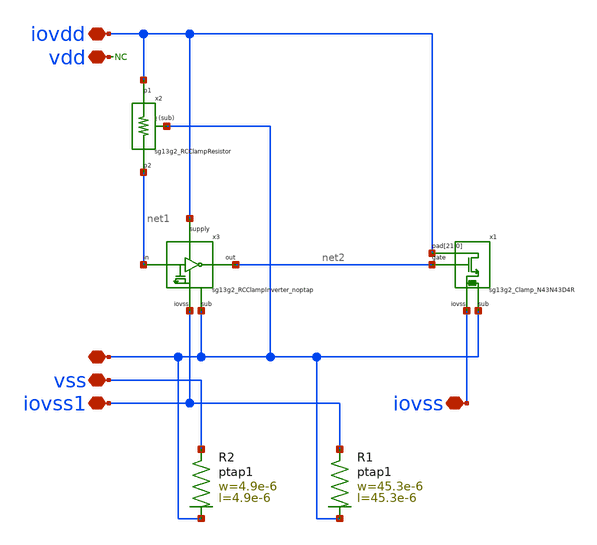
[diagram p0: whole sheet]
** sch_path: MSPHY6034-main/dependencies/unic_cass_2025_team04_padring/xschem/openpdk-libraries/ihp-sg13g2/sg13g2_io/xschem/sg13g2_IOPadIOVddAccess.sch
**.subckt sg13g2_IOPadIOVddAccess iovdd vss vdd ! iovss1 iovss
*.iopin iovdd
*.iopin vss
*.iopin vdd
*.iopin !
*.iopin iovss1
*.iopin iovss
XR2 vss ! ptap1 R=22.47 w=4.9e-6 l=4.9e-6
* noconn vdd
XR1 iovss1 ! ptap1 R=438.8m w=45.3e-6 l=45.3e-6
x1 iovss iovdd iovdd iovdd iovdd iovdd iovdd iovdd iovdd iovdd iovdd iovdd iovdd iovdd iovdd iovdd
+ iovdd iovdd iovdd iovdd iovdd iovdd iovdd ! net2 sg13g2_Clamp_N43N43D4R
x2 iovdd net1 ! sg13g2_RCClampResistor
x3 iovdd iovss1 net1 net2 ! sg13g2_RCClampInverter_noptap
**.ends
.end
